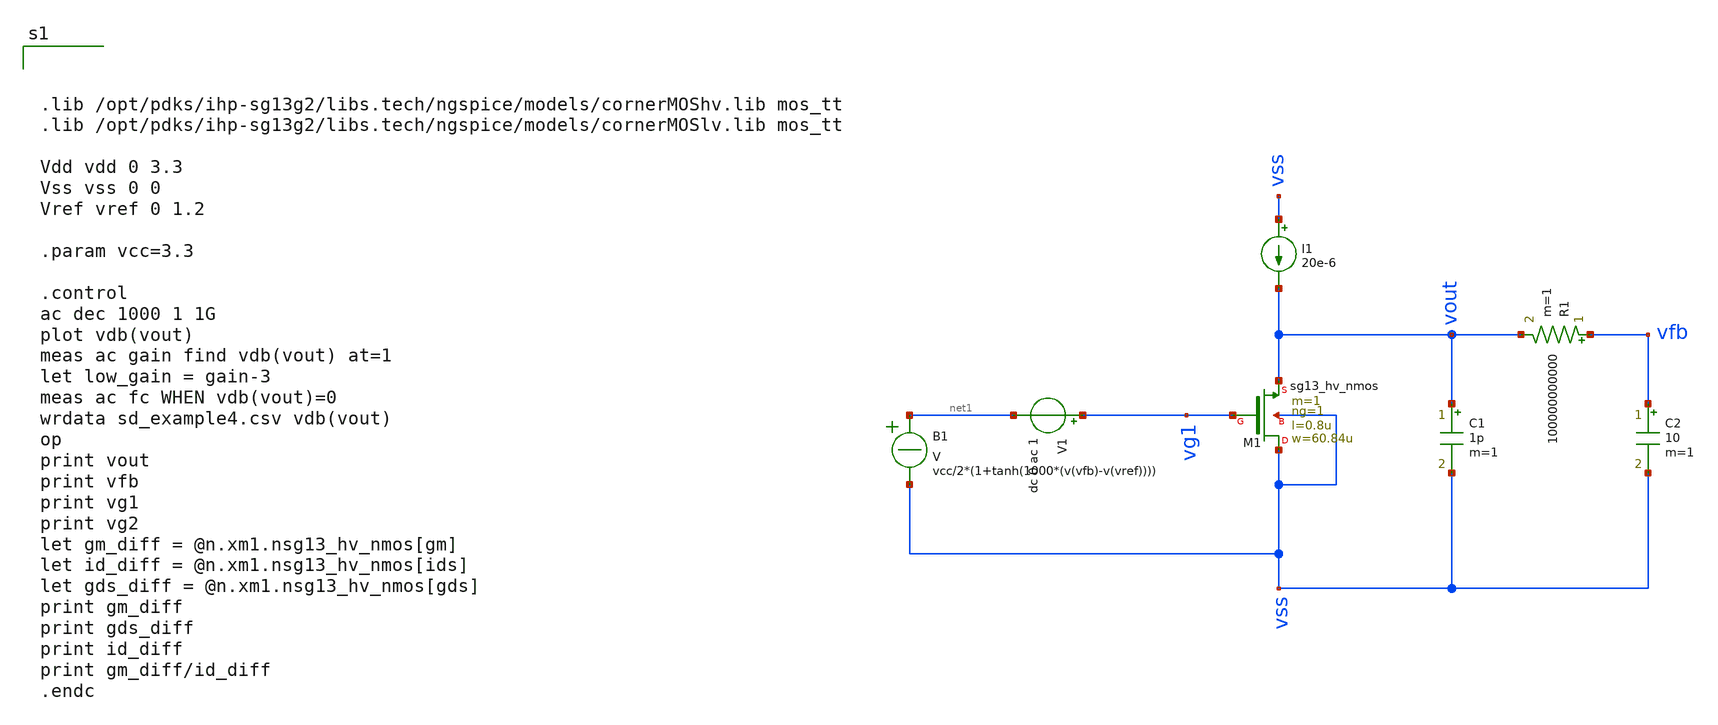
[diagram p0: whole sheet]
** sch_path: test/sstadex/xschem/sd_example4.sch
**.subckt sd_example4
XM1 vss vg1 vout vss sg13_hv_nmos w=60.84u l=0.8u ng=1 m=1 mm_ok=1
C1 vout vss 1p m=1
I1 vss vout 20e-6
B1 net1 vss V = vcc/2*(1+tanh(1000*(v(vfb)-v(vref))))
V1 vg1 net1 dc 0 ac 1
R1 vfb vout 100000000000 m=1
C2 vfb vss 10 m=1
**** begin user architecture code



.lib /opt/pdks/ihp-sg13g2/libs.tech/ngspice/models/cornerMOShv.lib mos_tt
.lib /opt/pdks/ihp-sg13g2/libs.tech/ngspice/models/cornerMOSlv.lib mos_tt

Vdd vdd 0 3.3
Vss vss 0 0
Vref vref 0 1.2

.param vcc=3.3

.control
ac dec 1000 1 1G
plot vdb(vout)
meas ac gain find vdb(vout) at=1
let low_gain = gain-3
meas ac fc WHEN vdb(vout)=0
wrdata sd_example4.csv vdb(vout)
op
print vout
print vfb
print vg1
print vg2
let gm_diff = @n.xm1.nsg13_hv_nmos[gm]
let id_diff = @n.xm1.nsg13_hv_nmos[ids]
let gds_diff = @n.xm1.nsg13_hv_nmos[gds]
print gm_diff
print gds_diff
print id_diff
print gm_diff/id_diff
.endc



**** end user architecture code
**.ends
.end
